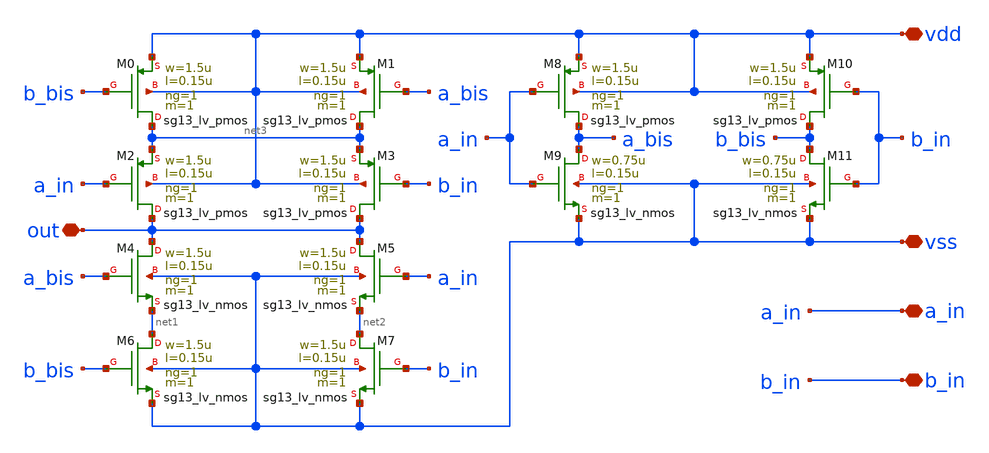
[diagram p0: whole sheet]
** sch_path: design/blocks/xorgate/schematic/xorgate.sch
**.subckt xorgate out vdd vss a_in b_in
*.iopin out
*.iopin vdd
*.iopin vss
*.iopin a_in
*.iopin b_in
XM0 net3 b_bis vdd vdd sg13_lv_pmos w=1.5u l=0.15u ng=1 m=1 mm_ok=1
XM1 net3 a_bis vdd vdd sg13_lv_pmos w=1.5u l=0.15u ng=1 m=1 mm_ok=1
XM2 out a_in net3 vdd sg13_lv_pmos w=1.5u l=0.15u ng=1 m=1 mm_ok=1
XM3 out b_in net3 vdd sg13_lv_pmos w=1.5u l=0.15u ng=1 m=1 mm_ok=1
XM4 out a_bis net1 vss sg13_lv_nmos w=1.5u l=0.15u ng=1 m=1 mm_ok=1
XM5 out a_in net2 vss sg13_lv_nmos w=1.5u l=0.15u ng=1 m=1 mm_ok=1
XM6 net1 b_bis vss vss sg13_lv_nmos w=1.5u l=0.15u ng=1 m=1 mm_ok=1
XM7 net2 b_in vss vss sg13_lv_nmos w=1.5u l=0.15u ng=1 m=1 mm_ok=1
XM8 a_bis a_in vdd vdd sg13_lv_pmos w=1.5u l=0.15u ng=1 m=1 mm_ok=1
XM9 a_bis a_in vss vss sg13_lv_nmos w=0.75u l=0.15u ng=1 m=1 mm_ok=1
XM10 b_bis b_in vdd vdd sg13_lv_pmos w=1.5u l=0.15u ng=1 m=1 mm_ok=1
XM11 b_bis b_in vss vss sg13_lv_nmos w=0.75u l=0.15u ng=1 m=1 mm_ok=1
**.ends
.end
